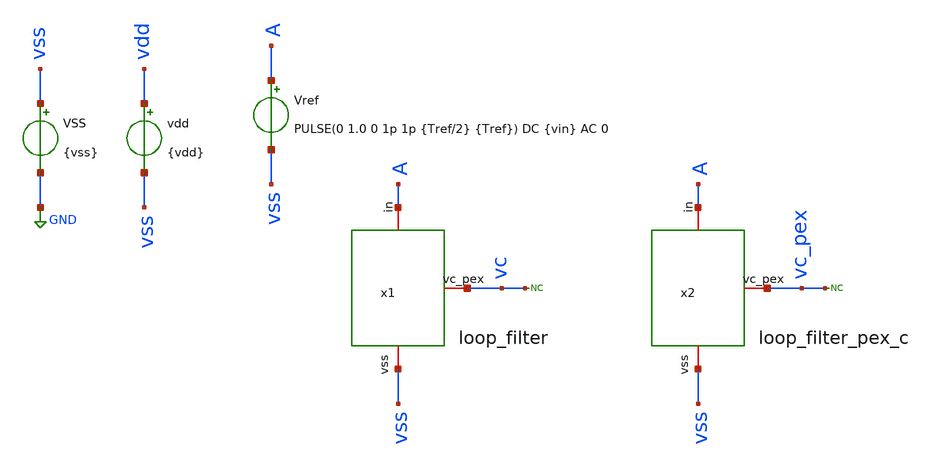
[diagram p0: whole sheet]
** sch_path: xschem/tb_loop_filter.sch
**.subckt tb_loop_filter
VSS vss GND {vss}
vdd vdd vss {vdd}
Vref A vss PULSE(0 1.0 0 1p 1p {Tref/2} {Tref}) DC {vin} AC 0
x1 vss A vc loop_filter
* noconn vc
* noconn vc_pex
x2 vss A vc_pex loop_filter_pex_c
**** begin user architecture code



* Parameters
.param kp = 1.0
.param vdd = kp*1.8
.param vss = 0.0
.param vin = vdd
.param fref = 5e6
.param Tref = 1/fref
.param iref = 100u
.param vd0 = 0.0
.param R1 = 1.6k
.param C1 = 33.5p
.param C2 = 6.7p

.options TEMP = 50.0
.options RSHUNT = 1e20

* Models
.lib ~/skywater/skywater-pdk/libraries/sky130_fd_pr_ngspice/latest/models/corners/sky130.lib TT
.include ~/caravel_analog_fulgor/xschem/simulations/loop_filter_pex_c.spice

* Data to save


* Simulation
.control

	tran 0.01ns 200ns
	meas tran t1 when v(vc)=0.63
	meas tran t2 when v(vc_pex)=0.63
	let R = t1/0.5p
	let Rpex = t2/05.p
	print R Rpex
	plot v(vc) v(vc_pex)
.endc
.end


**** end user architecture code
**.ends

* expanding   symbol:  loop_filter.sym # of pins=3
** sym_path: xschem/loop_filter.sym
** sch_path: xschem/loop_filter.sch
.subckt loop_filter vss in vc_pex
*.iopin in
*.iopin vss
*.iopin vc_pex
XC1 vc_pex vss sky130_fd_pr__cap_mim_m3_1 W=25 L=25 MF=25 m=25
XC2 in vss sky130_fd_pr__cap_mim_m3_1 W=20 L=20 MF=9 m=9
XR2 vc_pex net1 vss sky130_fd_pr__res_high_po_5p73 L=22.92 mult=1 m=1
XR1 vc_pex net1 vss sky130_fd_pr__res_high_po_5p73 L=22.92 mult=1 m=1
XR3 net1 in vss sky130_fd_pr__res_high_po_5p73 L=22.92 mult=1 m=1
.ends

.GLOBAL GND
.end
